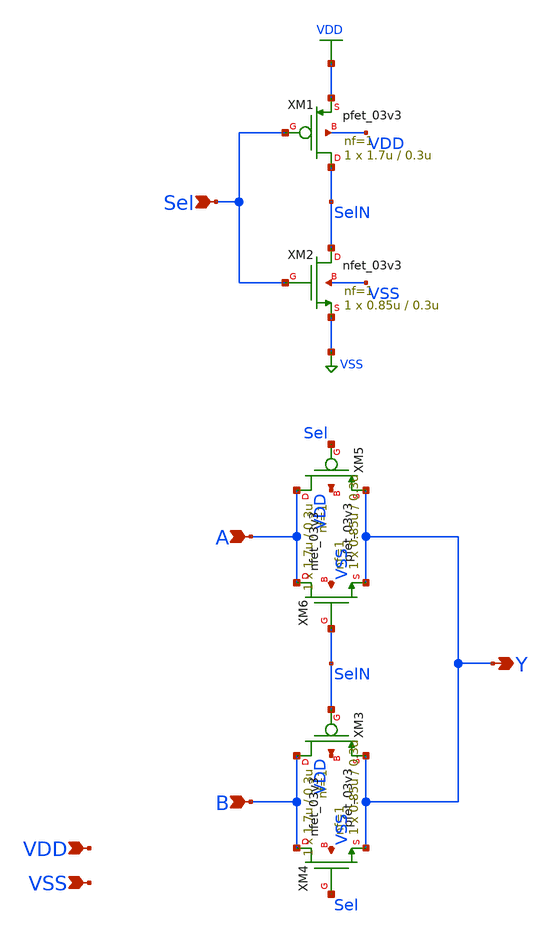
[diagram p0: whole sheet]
** sch_path: gf180mcu_osu_sc_gp9t3v3/xschem/gf180mcu_osu_sc_gp9t3v3__mux2_1.sch
**.subckt gf180mcu_osu_sc_gp9t3v3__mux2_1 A B Sel Y VDD VSS
*.ipin A
*.ipin B
*.ipin Sel
*.opin Y
*.ipin VDD
*.ipin VSS
XM1 SelN Sel VDD VDD pfet_03v3 L=0.3u W=1.7u nf=1 ad='int((nf+1)/2) * W/nf * 0.18u' as='int((nf+2)/2) * W/nf * 0.18u'
+ pd='2*int((nf+1)/2) * (W/nf + 0.18u)' ps='2*int((nf+2)/2) * (W/nf + 0.18u)' nrd='0.18u / W' nrs='0.18u / W'
+ sa=0 sb=0 sd=0 m=1
XM2 SelN Sel VSS VSS nfet_03v3 L=0.3u W=0.85u nf=1 ad='int((nf+1)/2) * W/nf * 0.18u' as='int((nf+2)/2) * W/nf * 0.18u'
+ pd='2*int((nf+1)/2) * (W/nf + 0.18u)' ps='2*int((nf+2)/2) * (W/nf + 0.18u)' nrd='0.18u / W' nrs='0.18u / W'
+ sa=0 sb=0 sd=0 m=1
XM3 B SelN Y VDD pfet_03v3 L=0.3u W=1.7u nf=1 ad='int((nf+1)/2) * W/nf * 0.18u' as='int((nf+2)/2) * W/nf * 0.18u'
+ pd='2*int((nf+1)/2) * (W/nf + 0.18u)' ps='2*int((nf+2)/2) * (W/nf + 0.18u)' nrd='0.18u / W' nrs='0.18u / W'
+ sa=0 sb=0 sd=0 m=1
XM4 B Sel Y VSS nfet_03v3 L=0.3u W=0.85u nf=1 ad='int((nf+1)/2) * W/nf * 0.18u' as='int((nf+2)/2) * W/nf * 0.18u'
+ pd='2*int((nf+1)/2) * (W/nf + 0.18u)' ps='2*int((nf+2)/2) * (W/nf + 0.18u)' nrd='0.18u / W' nrs='0.18u / W'
+ sa=0 sb=0 sd=0 m=1
XM5 A Sel Y VDD pfet_03v3 L=0.3u W=1.7u nf=1 ad='int((nf+1)/2) * W/nf * 0.18u' as='int((nf+2)/2) * W/nf * 0.18u'
+ pd='2*int((nf+1)/2) * (W/nf + 0.18u)' ps='2*int((nf+2)/2) * (W/nf + 0.18u)' nrd='0.18u / W' nrs='0.18u / W'
+ sa=0 sb=0 sd=0 m=1
XM6 A SelN Y VSS nfet_03v3 L=0.3u W=0.85u nf=1 ad='int((nf+1)/2) * W/nf * 0.18u' as='int((nf+2)/2) * W/nf * 0.18u'
+ pd='2*int((nf+1)/2) * (W/nf + 0.18u)' ps='2*int((nf+2)/2) * (W/nf + 0.18u)' nrd='0.18u / W' nrs='0.18u / W'
+ sa=0 sb=0 sd=0 m=1
**.ends
.GLOBAL VDD
.GLOBAL VSS
.end
